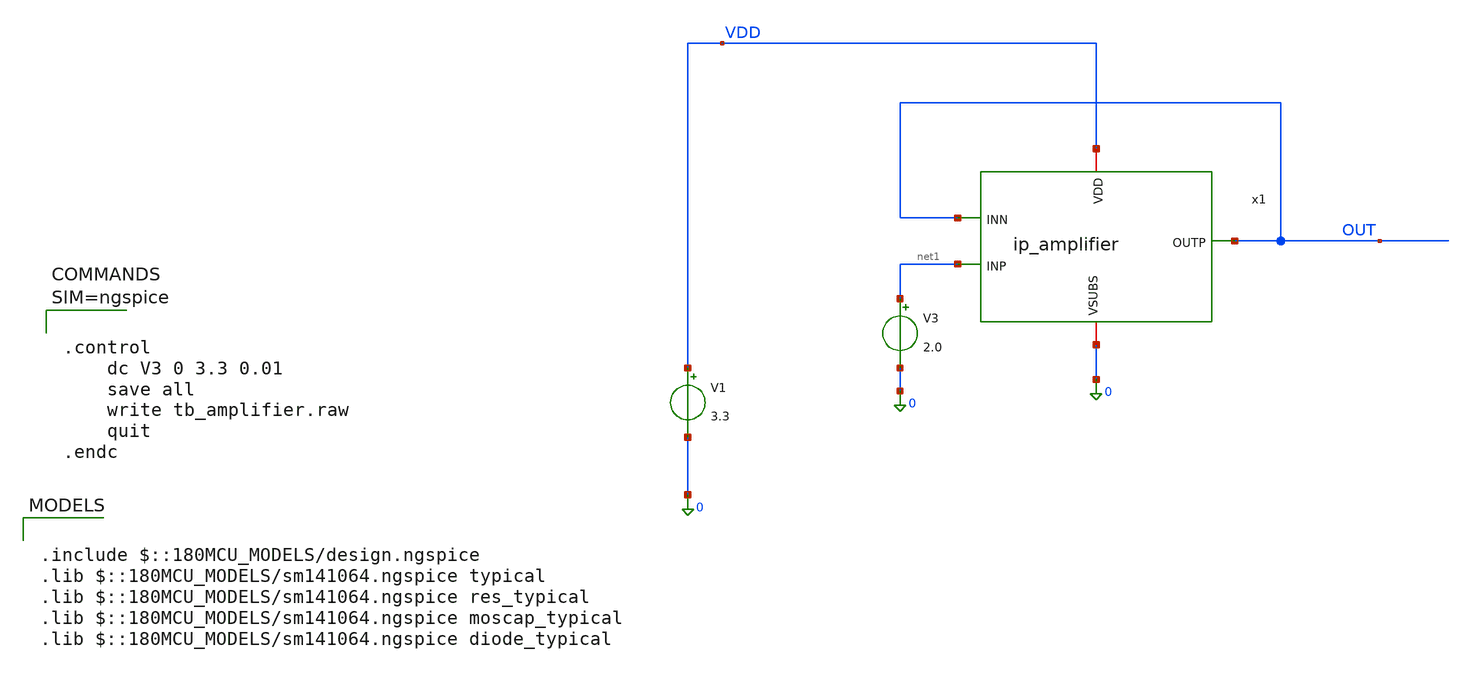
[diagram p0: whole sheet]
** sch_path: xschem/tb_amplifier.sch
**.subckt tb_amplifier
V1 VDD 0 3.3
x1 VDD OUT net1 OUT 0 ip_amplifier
V3 net1 0 2.0
**** begin user architecture code

.include $::180MCU_MODELS/design.ngspice
.lib $::180MCU_MODELS/sm141064.ngspice typical
.lib $::180MCU_MODELS/sm141064.ngspice res_typical
.lib $::180MCU_MODELS/sm141064.ngspice moscap_typical
.lib $::180MCU_MODELS/sm141064.ngspice diode_typical




.control
	dc V3 0 3.3 0.01
	save all
	write tb_amplifier.raw
	quit
.endc



**** end user architecture code
**.ends

* expanding   symbol:  ip_amplifier.sym # of pins=5
** sym_path: xschem/ip_amplifier.sym
** sch_path: xschem/ip_amplifier.sch
.subckt ip_amplifier VDD OUTP INP INN VSUBS
*.iopin VDD
*.iopin VSUBS
*.ipin INP
*.ipin INN
*.opin OUTP
XM1 net7 COM_P VDD VDD pfet_03v3 L=0.5u W=3.0u nf=1 ad='int((nf+1)/2) * W/nf * 0.18u' as='int((nf+2)/2) * W/nf * 0.18u'
+ pd='2*int((nf+1)/2) * (W/nf + 0.18u)' ps='2*int((nf+2)/2) * (W/nf + 0.18u)' nrd='0.18u / W' nrs='0.18u / W'
+ sa=0 sb=0 sd=0 m=1 par=1
XM2 net4 net2 net3 VSUBS nfet_03v3 L=2.0u W=10u nf=1 ad='int((nf+1)/2) * W/nf * 0.18u' as='int((nf+2)/2) * W/nf * 0.18u'
+ pd='2*int((nf+1)/2) * (W/nf + 0.18u)' ps='2*int((nf+2)/2) * (W/nf + 0.18u)' nrd='0.18u / W' nrs='0.18u / W'
+ sa=0 sb=0 sd=0 m=1 par=1
XM3 net3 net2 VSUBS VSUBS nfet_03v3 L=0.5u W=1.0u nf=1 ad='int((nf+1)/2) * W/nf * 0.18u' as='int((nf+2)/2) * W/nf * 0.18u'
+ pd='2*int((nf+1)/2) * (W/nf + 0.18u)' ps='2*int((nf+2)/2) * (W/nf + 0.18u)' nrd='0.18u / W' nrs='0.18u / W'
+ sa=0 sb=0 sd=0 m=1 par=1
XM4 net1 net2 VSUBS VSUBS nfet_03v3 L=0.5u W=1.0u nf=1 ad='int((nf+1)/2) * W/nf * 0.18u' as='int((nf+2)/2) * W/nf * 0.18u'
+ pd='2*int((nf+1)/2) * (W/nf + 0.18u)' ps='2*int((nf+2)/2) * (W/nf + 0.18u)' nrd='0.18u / W' nrs='0.18u / W'
+ sa=0 sb=0 sd=0 m=1 par=1
XM5 net5 COM_P VDD VDD pfet_03v3 L=0.5u W=3.0u nf=1 ad='int((nf+1)/2) * W/nf * 0.18u' as='int((nf+2)/2) * W/nf * 0.18u'
+ pd='2*int((nf+1)/2) * (W/nf + 0.18u)' ps='2*int((nf+2)/2) * (W/nf + 0.18u)' nrd='0.18u / W' nrs='0.18u / W'
+ sa=0 sb=0 sd=0 m=1 par=1
XM6 net6 COM_P net5 VDD pfet_03v3 L=2.0u W=10.0u nf=1 ad='int((nf+1)/2) * W/nf * 0.18u' as='int((nf+2)/2) * W/nf * 0.18u'
+ pd='2*int((nf+1)/2) * (W/nf + 0.18u)' ps='2*int((nf+2)/2) * (W/nf + 0.18u)' nrd='0.18u / W' nrs='0.18u / W'
+ sa=0 sb=0 sd=0 m=1 par=1
XM7 DIFF_L COM_P VDD VDD pfet_03v3 L=0.5u W=3.0u nf=1 ad='int((nf+1)/2) * W/nf * 0.18u' as='int((nf+2)/2) * W/nf * 0.18u'
+ pd='2*int((nf+1)/2) * (W/nf + 0.18u)' ps='2*int((nf+2)/2) * (W/nf + 0.18u)' nrd='0.18u / W' nrs='0.18u / W'
+ sa=0 sb=0 sd=0 m=1 par=1
XM9 DIFF_R COM_P VDD VDD pfet_03v3 L=0.5u W=3.0u nf=1 ad='int((nf+1)/2) * W/nf * 0.18u' as='int((nf+2)/2) * W/nf * 0.18u'
+ pd='2*int((nf+1)/2) * (W/nf + 0.18u)' ps='2*int((nf+2)/2) * (W/nf + 0.18u)' nrd='0.18u / W' nrs='0.18u / W'
+ sa=0 sb=0 sd=0 m=1 par=1
XM11 net10 INP net4 VSUBS nfet_03v3 L=0.3u W=4.0u nf=1 ad='int((nf+1)/2) * W/nf * 0.18u' as='int((nf+2)/2) * W/nf * 0.18u'
+ pd='2*int((nf+1)/2) * (W/nf + 0.18u)' ps='2*int((nf+2)/2) * (W/nf + 0.18u)' nrd='0.18u / W' nrs='0.18u / W'
+ sa=0 sb=0 sd=0 m=2 par=2
XM12 net11 INN net4 VSUBS nfet_03v3 L=0.3u W=4.0u nf=1 ad='int((nf+1)/2) * W/nf * 0.18u' as='int((nf+2)/2) * W/nf * 0.18u'
+ pd='2*int((nf+1)/2) * (W/nf + 0.18u)' ps='2*int((nf+2)/2) * (W/nf + 0.18u)' nrd='0.18u / W' nrs='0.18u / W'
+ sa=0 sb=0 sd=0 m=2 par=2
XM8 net8 COM_P DIFF_L VDD pfet_03v3 L=2.0u W=10.0u nf=1 ad='int((nf+1)/2) * W/nf * 0.18u' as='int((nf+2)/2) * W/nf * 0.18u'
+ pd='2*int((nf+1)/2) * (W/nf + 0.18u)' ps='2*int((nf+2)/2) * (W/nf + 0.18u)' nrd='0.18u / W' nrs='0.18u / W'
+ sa=0 sb=0 sd=0 m=1 par=1
XM10 net9 COM_P DIFF_R VDD pfet_03v3 L=2.0u W=10.0u nf=1 ad='int((nf+1)/2) * W/nf * 0.18u' as='int((nf+2)/2) * W/nf * 0.18u'
+ pd='2*int((nf+1)/2) * (W/nf + 0.18u)' ps='2*int((nf+2)/2) * (W/nf + 0.18u)' nrd='0.18u / W' nrs='0.18u / W'
+ sa=0 sb=0 sd=0 m=1 par=1
XM13 LOW_R LOW_L VSUBS VSUBS nfet_03v3 L=0.3u W=2.0u nf=1 ad='int((nf+1)/2) * W/nf * 0.18u' as='int((nf+2)/2) * W/nf * 0.18u'
+ pd='2*int((nf+1)/2) * (W/nf + 0.18u)' ps='2*int((nf+2)/2) * (W/nf + 0.18u)' nrd='0.18u / W' nrs='0.18u / W'
+ sa=0 sb=0 sd=0 m=1 par=1
XM14 LOW_L LOW_L VSUBS VSUBS nfet_03v3 L=0.3u W=2.0u nf=1 ad='int((nf+1)/2) * W/nf * 0.18u' as='int((nf+2)/2) * W/nf * 0.18u'
+ pd='2*int((nf+1)/2) * (W/nf + 0.18u)' ps='2*int((nf+2)/2) * (W/nf + 0.18u)' nrd='0.18u / W' nrs='0.18u / W'
+ sa=0 sb=0 sd=0 m=1 par=1
XM15 net13 COM_P VDD VDD pfet_03v3 L=0.5u W=9u nf=1 ad='int((nf+1)/2) * W/nf * 0.18u' as='int((nf+2)/2) * W/nf * 0.18u'
+ pd='2*int((nf+1)/2) * (W/nf + 0.18u)' ps='2*int((nf+2)/2) * (W/nf + 0.18u)' nrd='0.18u / W' nrs='0.18u / W'
+ sa=0 sb=0 sd=0 m=5 par=5
XM16 net14 LOW_R VSUBS VSUBS nfet_03v3 L=0.5u W=5.0u nf=1 ad='int((nf+1)/2) * W/nf * 0.18u' as='int((nf+2)/2) * W/nf * 0.18u'
+ pd='2*int((nf+1)/2) * (W/nf + 0.18u)' ps='2*int((nf+2)/2) * (W/nf + 0.18u)' nrd='0.18u / W' nrs='0.18u / W'
+ sa=0 sb=0 sd=0 m=5 par=5
R1 COM_P net12 100k m=1
Vmeas net12 VSUBS 0
Vmeas1 net6 net2 0
Vmeas2 net8 LOW_L 0
Vmeas3 net9 LOW_R 0
Vmeas4 DIFF_R net11 0
Vmeas5 DIFF_L net10 0
C1 OUTP LOW_R 0.5p m=1
XM17 COM_P COM_P net7 VDD pfet_03v3 L=2.0u W=10.0u nf=1 ad='int((nf+1)/2) * W/nf * 0.18u' as='int((nf+2)/2) * W/nf * 0.18u'
+ pd='2*int((nf+1)/2) * (W/nf + 0.18u)' ps='2*int((nf+2)/2) * (W/nf + 0.18u)' nrd='0.18u / W' nrs='0.18u / W'
+ sa=0 sb=0 sd=0 m=1 par=1
XM18 net2 net2 net1 VSUBS nfet_03v3 L=2.0u W=10u nf=1 ad='int((nf+1)/2) * W/nf * 0.18u' as='int((nf+2)/2) * W/nf * 0.18u'
+ pd='2*int((nf+1)/2) * (W/nf + 0.18u)' ps='2*int((nf+2)/2) * (W/nf + 0.18u)' nrd='0.18u / W' nrs='0.18u / W'
+ sa=0 sb=0 sd=0 m=1 par=1
Vmeas6 net13 OUTP 0
Vmeas7 OUTP net14 0
.ends

.end
